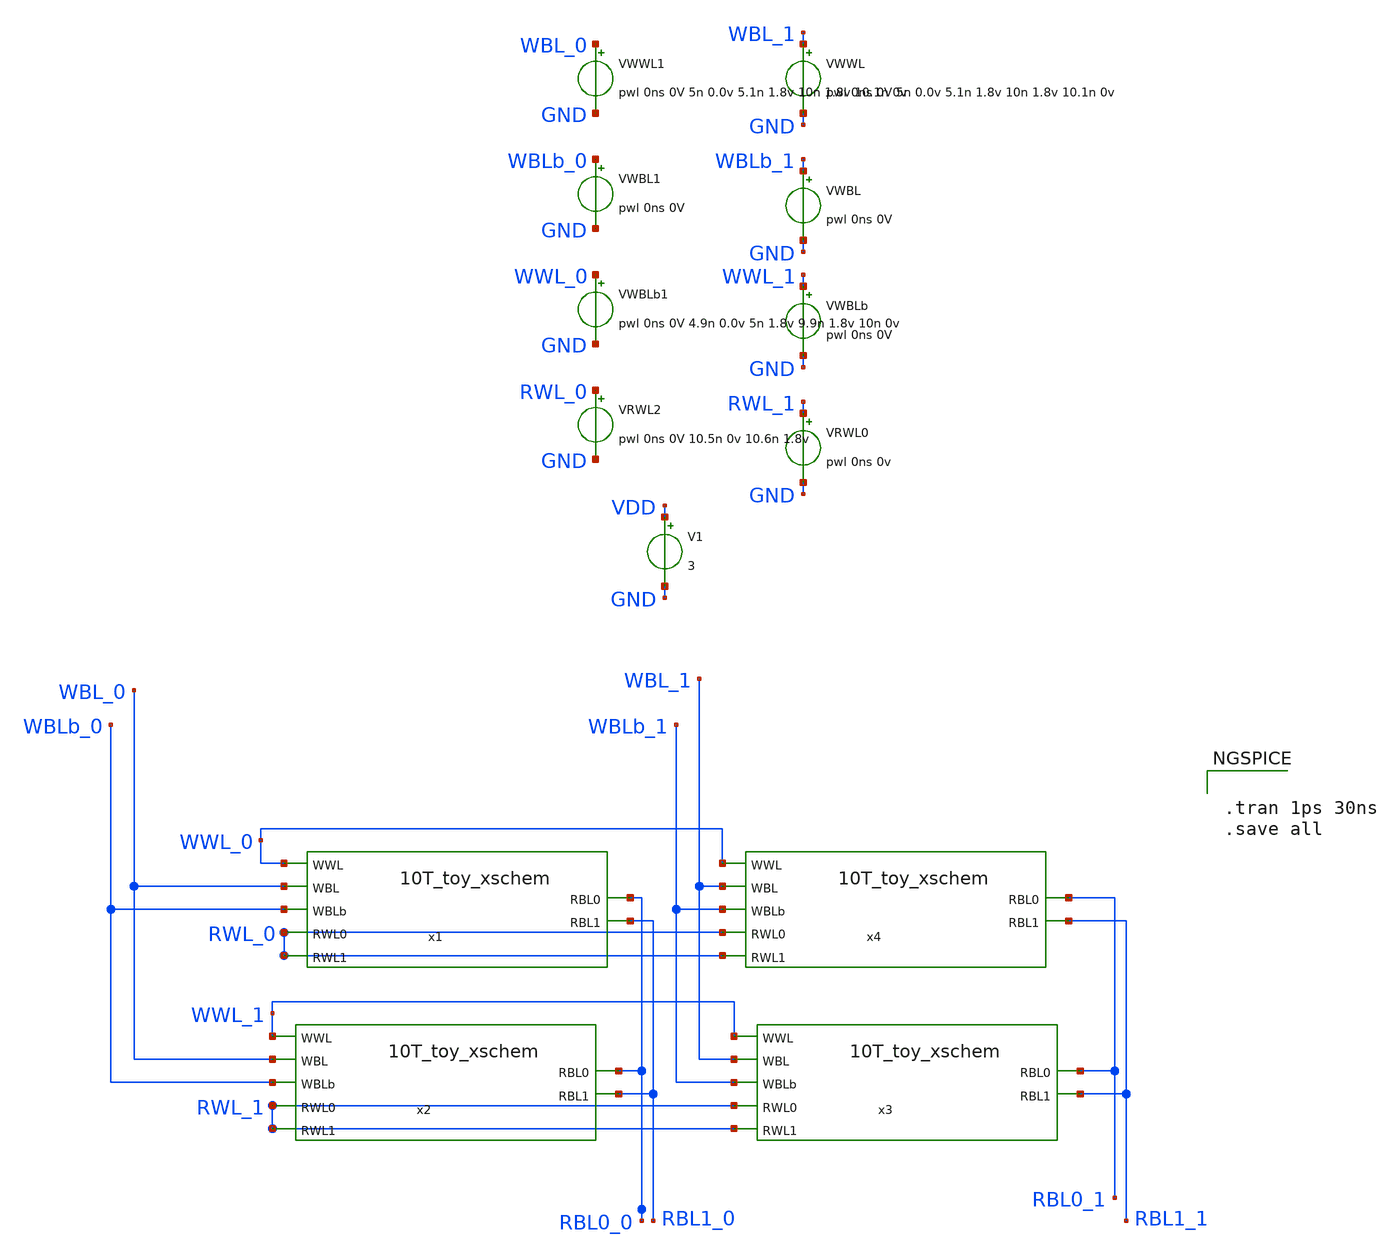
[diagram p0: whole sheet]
** sch_path: custom/xschem/10T_4x4_xschem.sch
**.subckt 10T_4x4_xschem
x1 WWL_0 WBL_0 RBL0_0 RBL1_0 WBLb_0 RWL_0 RWL_0 VDD GND 10T_toy_xschem
x2 WWL_1 WBL_0 RBL0_0 RBL1_0 WBLb_0 RWL_1 RWL_1 VDD GND 10T_toy_xschem
x3 WWL_1 WBL_1 RBL0_1 RBL1_1 WBLb_1 RWL_1 RWL_1 VDD GND 10T_toy_xschem
x4 WWL_0 WBL_1 RBL0_1 RBL1_1 WBLb_1 RWL_0 RWL_0 VDD GND 10T_toy_xschem
V1 VDD GND 3
VWWL WBL_1 GND pwl 0ns 0V 5n 0.0v 5.1n 1.8v 10n 1.8v 10.1n 0v
VWBL WBLb_1 GND pwl 0ns 0V
VWBLb WWL_1 GND pwl 0ns 0V
VRWL0 RWL_1 GND pwl 0ns 0v
VWWL1 WBL_0 GND pwl 0ns 0V 5n 0.0v 5.1n 1.8v 10n 1.8v 10.1n 0v
VWBL1 WBLb_0 GND pwl 0ns 0V
VWBLb1 WWL_0 GND pwl 0ns 0V 4.9n 0.0v 5n 1.8v 9.9n 1.8v 10n 0v
VRWL2 RWL_0 GND pwl 0ns 0V 10.5n 0v 10.6n 1.8v
**** begin user architecture code

.lib $::SKYWATER_MODELS/sky130.lib.spice tt


**** end user architecture code
**.ends

* expanding   symbol:  10T_toy_xschem.sym # of pins=7
** sym_path: custom/xschem/10T_toy_xschem.sym
** sch_path: custom/xschem/10T_toy_xschem.sch
.subckt 10T_toy_xschem WWL WBL RBL0 RBL1 WBLb RWL0 RWL1 VDD GND
*.ipin WWL
*.ipin RWL0
*.ipin RWL1
*.ipin WBL
*.ipin WBLb
*.opin RBL0
*.opin RBL1
x1 net1 net2 VDD GND INVX1
x2 net2 net1 VDD GND INVX1
XM1 net2 WWL WBL GND sky130_fd_pr__nfet_01v8 L=0.15 W=0.14 nf=1 ad='int((nf+1)/2) * W/nf * 0.29' as='int((nf+2)/2) * W/nf * 0.29'
+ pd='2*int((nf+1)/2) * (W/nf + 0.29)' ps='2*int((nf+2)/2) * (W/nf + 0.29)' nrd='0.29 / W' nrs='0.29 / W'
+ sa=0 sb=0 sd=0 mult=1 m=1
XM2 WBLb WWL net1 GND sky130_fd_pr__nfet_01v8 L=0.15 W=0.14 nf=1 ad='int((nf+1)/2) * W/nf * 0.29' as='int((nf+2)/2) * W/nf * 0.29'
+ pd='2*int((nf+1)/2) * (W/nf + 0.29)' ps='2*int((nf+2)/2) * (W/nf + 0.29)' nrd='0.29 / W' nrs='0.29 / W'
+ sa=0 sb=0 sd=0 mult=1 m=1
XM3 net3 net2 GND GND sky130_fd_pr__nfet_01v8 L=0.15 W=0.14 nf=1 ad='int((nf+1)/2) * W/nf * 0.29' as='int((nf+2)/2) * W/nf * 0.29'
+ pd='2*int((nf+1)/2) * (W/nf + 0.29)' ps='2*int((nf+2)/2) * (W/nf + 0.29)' nrd='0.29 / W' nrs='0.29 / W'
+ sa=0 sb=0 sd=0 mult=1 m=1
XM4 RBL0 RWL0 net3 GND sky130_fd_pr__nfet_01v8 L=0.15 W=0.21 nf=1 ad='int((nf+1)/2) * W/nf * 0.29' as='int((nf+2)/2) * W/nf * 0.29'
+ pd='2*int((nf+1)/2) * (W/nf + 0.29)' ps='2*int((nf+2)/2) * (W/nf + 0.29)' nrd='0.29 / W' nrs='0.29 / W'
+ sa=0 sb=0 sd=0 mult=1 m=1
XM5 net4 net1 GND GND sky130_fd_pr__nfet_01v8 L=0.15 W=0.14 nf=1 ad='int((nf+1)/2) * W/nf * 0.29' as='int((nf+2)/2) * W/nf * 0.29'
+ pd='2*int((nf+1)/2) * (W/nf + 0.29)' ps='2*int((nf+2)/2) * (W/nf + 0.29)' nrd='0.29 / W' nrs='0.29 / W'
+ sa=0 sb=0 sd=0 mult=1 m=1
XM6 RBL1 RWL1 net4 GND sky130_fd_pr__nfet_01v8 L=0.15 W=0.21 nf=1 ad='int((nf+1)/2) * W/nf * 0.29' as='int((nf+2)/2) * W/nf * 0.29'
+ pd='2*int((nf+1)/2) * (W/nf + 0.29)' ps='2*int((nf+2)/2) * (W/nf + 0.29)' nrd='0.29 / W' nrs='0.29 / W'
+ sa=0 sb=0 sd=0 mult=1 m=1
.ends


* expanding   symbol:  INVX1.sym # of pins=2
** sym_path: custom/xschem/INVX1.sym
** sch_path: custom/xschem/INVX1.sch
.subckt INVX1 Y A VDD GND
*.ipin A
*.opin Y
XM1 Y A GND GND sky130_fd_pr__nfet_01v8 L=0.15 W=0.21 nf=1 ad='int((nf+1)/2) * W/nf * 0.29' as='int((nf+2)/2) * W/nf * 0.29'
+ pd='2*int((nf+1)/2) * (W/nf + 0.29)' ps='2*int((nf+2)/2) * (W/nf + 0.29)' nrd='0.29 / W' nrs='0.29 / W'
+ sa=0 sb=0 sd=0 mult=1 m=1
XM2 Y A VDD VDD sky130_fd_pr__pfet_01v8 L=0.15 W=0.14 nf=1 ad='int((nf+1)/2) * W/nf * 0.29' as='int((nf+2)/2) * W/nf * 0.29'
+ pd='2*int((nf+1)/2) * (W/nf + 0.29)' ps='2*int((nf+2)/2) * (W/nf + 0.29)' nrd='0.29 / W' nrs='0.29 / W'
+ sa=0 sb=0 sd=0 mult=1 m=1
.ends

**** begin user architecture code


.tran 1ps 30ns
.save all



**** end user architecture code
.end
